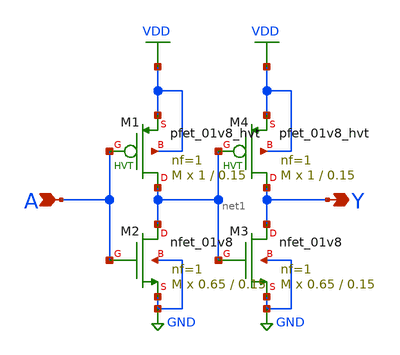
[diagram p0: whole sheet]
** sch_path: designs/buffer.sch
**.subckt buffer A Y
*.ipin A
*.opin Y
XM2 net1 A GND GND sky130_fd_pr__nfet_01v8 L=0.15 W=0.65 nf=1 ad='int((nf+1)/2) * W/nf * 0.29' as='int((nf+2)/2) * W/nf * 0.29'
+ pd='2*int((nf+1)/2) * (W/nf + 0.29)' ps='2*int((nf+2)/2) * (W/nf + 0.29)' nrd='0.29 / W' nrs='0.29 / W'
+ sa=0 sb=0 sd=0 mult=M m=M
XM1 net1 A VDD VDD sky130_fd_pr__pfet_01v8_hvt L=0.15 W=1 nf=1 ad='int((nf+1)/2) * W/nf * 0.29' as='int((nf+2)/2) * W/nf * 0.29'
+ pd='2*int((nf+1)/2) * (W/nf + 0.29)' ps='2*int((nf+2)/2) * (W/nf + 0.29)' nrd='0.29 / W' nrs='0.29 / W'
+ sa=0 sb=0 sd=0 mult=M m=M
XM3 Y net1 GND GND sky130_fd_pr__nfet_01v8 L=0.15 W=0.65 nf=1 ad='int((nf+1)/2) * W/nf * 0.29' as='int((nf+2)/2) * W/nf * 0.29'
+ pd='2*int((nf+1)/2) * (W/nf + 0.29)' ps='2*int((nf+2)/2) * (W/nf + 0.29)' nrd='0.29 / W' nrs='0.29 / W'
+ sa=0 sb=0 sd=0 mult=M m=M
XM4 Y net1 VDD VDD sky130_fd_pr__pfet_01v8_hvt L=0.15 W=1 nf=1 ad='int((nf+1)/2) * W/nf * 0.29' as='int((nf+2)/2) * W/nf * 0.29'
+ pd='2*int((nf+1)/2) * (W/nf + 0.29)' ps='2*int((nf+2)/2) * (W/nf + 0.29)' nrd='0.29 / W' nrs='0.29 / W'
+ sa=0 sb=0 sd=0 mult=M m=M
**.ends
.GLOBAL GND
.GLOBAL VDD
.end
